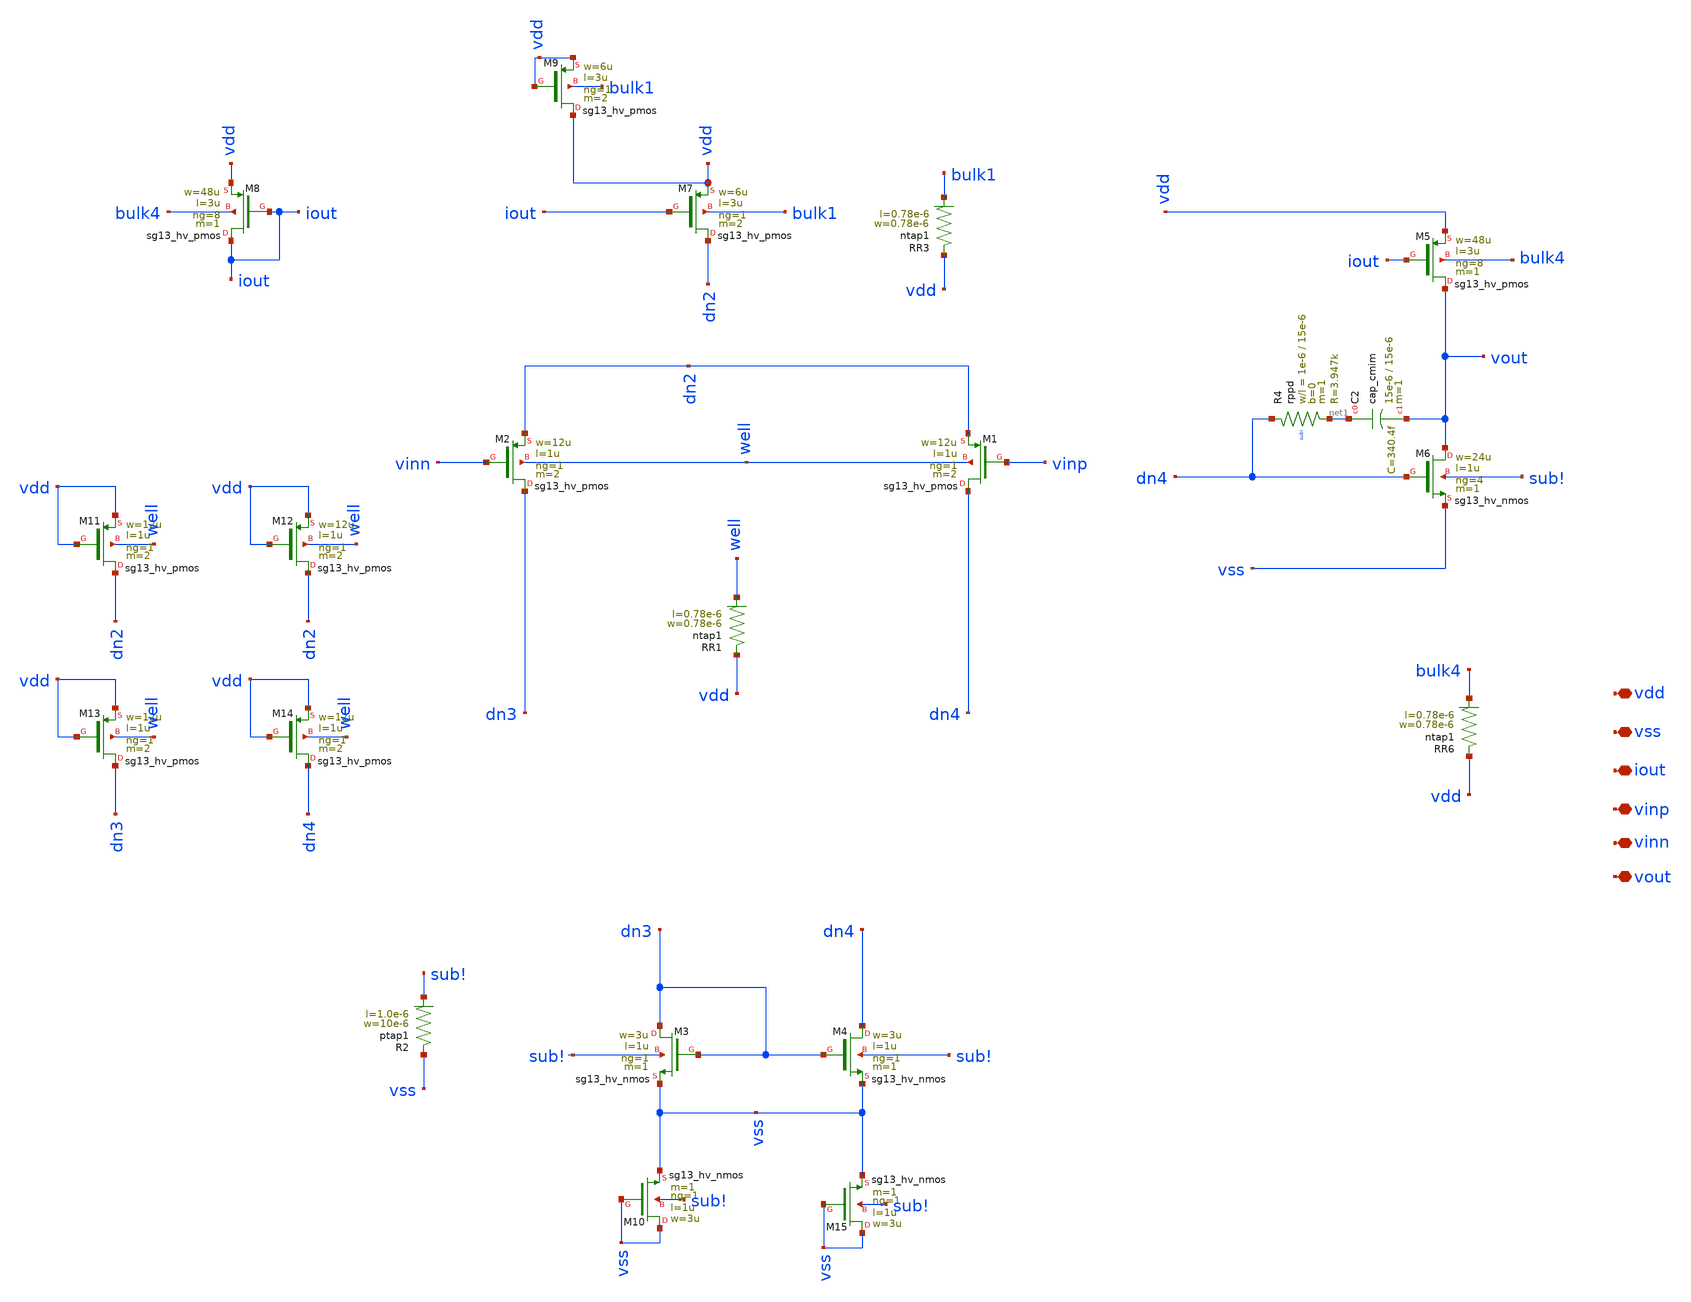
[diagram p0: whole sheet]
** sch_path: dependencies/pmu_ip/dependencies/OTA/OTA-main/schematic/xschem/ota_layout.sch
**.subckt ota_layout vdd vss iout vinp vinn vout
*.iopin vdd
*.iopin vss
*.iopin iout
*.iopin vinp
*.iopin vinn
*.iopin vout
XM1 dn4 vinp dn2 well sg13_hv_pmos w=12u l=1u ng=1 m=2 mm_ok=1
XM2 dn3 vinn dn2 well sg13_hv_pmos w=12u l=1u ng=1 m=2 mm_ok=1
XM11 dn2 vdd vdd well sg13_hv_pmos w=12u l=1u ng=1 m=2 mm_ok=1
XM12 dn2 vdd vdd well sg13_hv_pmos w=12u l=1u ng=1 m=2 mm_ok=1
XM13 dn3 vdd vdd well sg13_hv_pmos w=12u l=1u ng=1 m=2 mm_ok=1
XM14 dn4 vdd vdd well sg13_hv_pmos w=12u l=1u ng=1 m=2 mm_ok=1
XR1 vdd well ntap1 R=262.8 w=0.78e-6 l=0.78e-6
XR2 vss sub! ptap1 R=30.62 w=10e-6 l=1.0e-6
XR3 vdd bulk1 ntap1 R=262.8 w=0.78e-6 l=0.78e-6
XC2 net1 vout cap_cmim w=15e-6 l=15e-6 m=1 mm_ok=1
XR4 dn4 net1 sub! rppd w=1e-6 l=15e-6 m=1 b=0 mm_ok=1
XR6 vdd bulk4 ntap1 R=262.8 w=0.78e-6 l=0.78e-6
XM5 vout iout vdd bulk4 sg13_hv_pmos w=48u l=3u ng=8 m=1 mm_ok=1
XM6 vout dn4 vss sub! sg13_hv_nmos w=24u l=1u ng=4 m=1 mm_ok=1
XM7 dn2 iout vdd bulk1 sg13_hv_pmos w=6u l=3u ng=1 m=2 mm_ok=1
XM8 iout iout vdd bulk4 sg13_hv_pmos w=48u l=3u ng=8 m=1 mm_ok=1
XM3 dn3 dn3 vss sub! sg13_hv_nmos w=3u l=1u ng=1 m=1 mm_ok=1
XM4 dn4 dn3 vss sub! sg13_hv_nmos w=3u l=1u ng=1 m=1 mm_ok=1
XM9 vdd vdd vdd bulk1 sg13_hv_pmos w=6u l=3u ng=1 m=2 mm_ok=1
XM10 vss vss vss sub! sg13_hv_nmos w=3u l=1u ng=1 m=1 mm_ok=1
XM15 vss vss vss sub! sg13_hv_nmos w=3u l=1u ng=1 m=1 mm_ok=1
**.ends
.end
